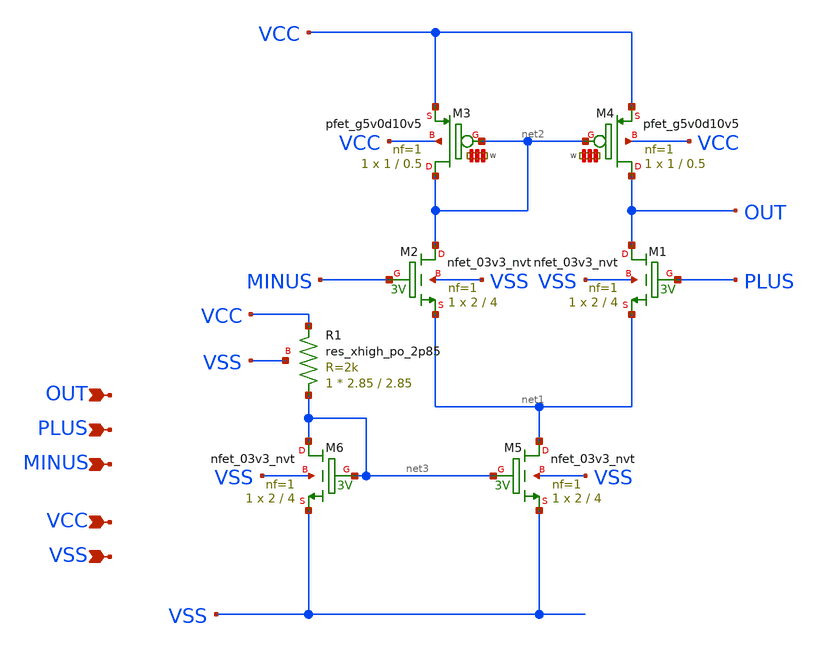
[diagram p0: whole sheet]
** sch_path: xschem/untitled.sch
**.subckt untitled OUT PLUS MINUS VCC VSS
*.ipin OUT
*.ipin PLUS
*.ipin MINUS
*.ipin VCC
*.ipin VSS
XM1 OUT PLUS net1 VSS sky130_fd_pr__nfet_03v3_nvt L=4 W=2 nf=1 ad='int((nf+1)/2) * W/nf * 0.29' as='int((nf+2)/2) * W/nf * 0.29'
+ pd='2*int((nf+1)/2) * (W/nf + 0.29)' ps='2*int((nf+2)/2) * (W/nf + 0.29)' nrd='0.29 / W' nrs='0.29 / W'
+ sa=0 sb=0 sd=0 mult=1 m=1
XM2 net2 MINUS net1 VSS sky130_fd_pr__nfet_03v3_nvt L=4 W=2 nf=1 ad='int((nf+1)/2) * W/nf * 0.29' as='int((nf+2)/2) * W/nf * 0.29'
+ pd='2*int((nf+1)/2) * (W/nf + 0.29)' ps='2*int((nf+2)/2) * (W/nf + 0.29)' nrd='0.29 / W' nrs='0.29 / W'
+ sa=0 sb=0 sd=0 mult=1 m=1
XM3 net2 net2 VCC VCC sky130_fd_pr__pfet_g5v0d10v5 L=0.5 W='1 * 1 ' nf=1 ad='int((nf+1)/2) * W / nf * 0.29'
+ as='int((nf+2)/2) * W / nf * 0.29' pd='2*int((nf+1)/2) * (W / nf + 0.29)' ps='2*int((nf+2)/2) * (W / nf + 0.29)'
+ nrd='0.29 / W ' nrs='0.29 / W ' sa=0 sb=0 sd=0 mult=1 m=1
XM4 OUT net2 VCC VCC sky130_fd_pr__pfet_g5v0d10v5 L=0.5 W='1 * 1 ' nf=1 ad='int((nf+1)/2) * W / nf * 0.29'
+ as='int((nf+2)/2) * W / nf * 0.29' pd='2*int((nf+1)/2) * (W / nf + 0.29)' ps='2*int((nf+2)/2) * (W / nf + 0.29)'
+ nrd='0.29 / W ' nrs='0.29 / W ' sa=0 sb=0 sd=0 mult=1 m=1
XM5 net1 net3 VSS VSS sky130_fd_pr__nfet_03v3_nvt L=4 W=2 nf=1 ad='int((nf+1)/2) * W/nf * 0.29' as='int((nf+2)/2) * W/nf * 0.29'
+ pd='2*int((nf+1)/2) * (W/nf + 0.29)' ps='2*int((nf+2)/2) * (W/nf + 0.29)' nrd='0.29 / W' nrs='0.29 / W'
+ sa=0 sb=0 sd=0 mult=1 m=1
XM6 net3 net3 VSS VSS sky130_fd_pr__nfet_03v3_nvt L=4 W=2 nf=1 ad='int((nf+1)/2) * W/nf * 0.29' as='int((nf+2)/2) * W/nf * 0.29'
+ pd='2*int((nf+1)/2) * (W/nf + 0.29)' ps='2*int((nf+2)/2) * (W/nf + 0.29)' nrd='0.29 / W' nrs='0.29 / W'
+ sa=0 sb=0 sd=0 mult=1 m=1
XR1 net3 VCC VSS sky130_fd_pr__res_xhigh_po_2p85 L=2.85 mult=1 m=1
**.ends
.end
